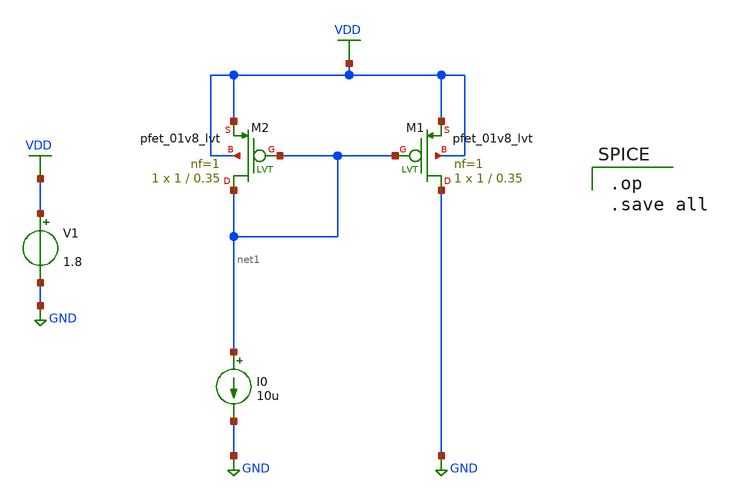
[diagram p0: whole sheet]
** sch_path: xschem/untitled-1.sch
**.subckt untitled-1
XM1 GND net1 VDD VDD sky130_fd_pr__pfet_01v8_lvt L=0.35 W=1 nf=1 ad='int((nf+1)/2) * W/nf * 0.29' as='int((nf+2)/2) * W/nf * 0.29'
+ pd='2*int((nf+1)/2) * (W/nf + 0.29)' ps='2*int((nf+2)/2) * (W/nf + 0.29)' nrd='0.29 / W' nrs='0.29 / W'
+ sa=0 sb=0 sd=0 mult=1 m=1
XM2 net1 net1 VDD VDD sky130_fd_pr__pfet_01v8_lvt L=0.35 W=1 nf=1 ad='int((nf+1)/2) * W/nf * 0.29' as='int((nf+2)/2) * W/nf * 0.29'
+ pd='2*int((nf+1)/2) * (W/nf + 0.29)' ps='2*int((nf+2)/2) * (W/nf + 0.29)' nrd='0.29 / W' nrs='0.29 / W'
+ sa=0 sb=0 sd=0 mult=1 m=1
I0 net1 GND 10u
V1 VDD GND 1.8
**** begin user architecture code

.op
.save all

**** end user architecture code
**.ends
.GLOBAL GND
.GLOBAL VDD
.end
